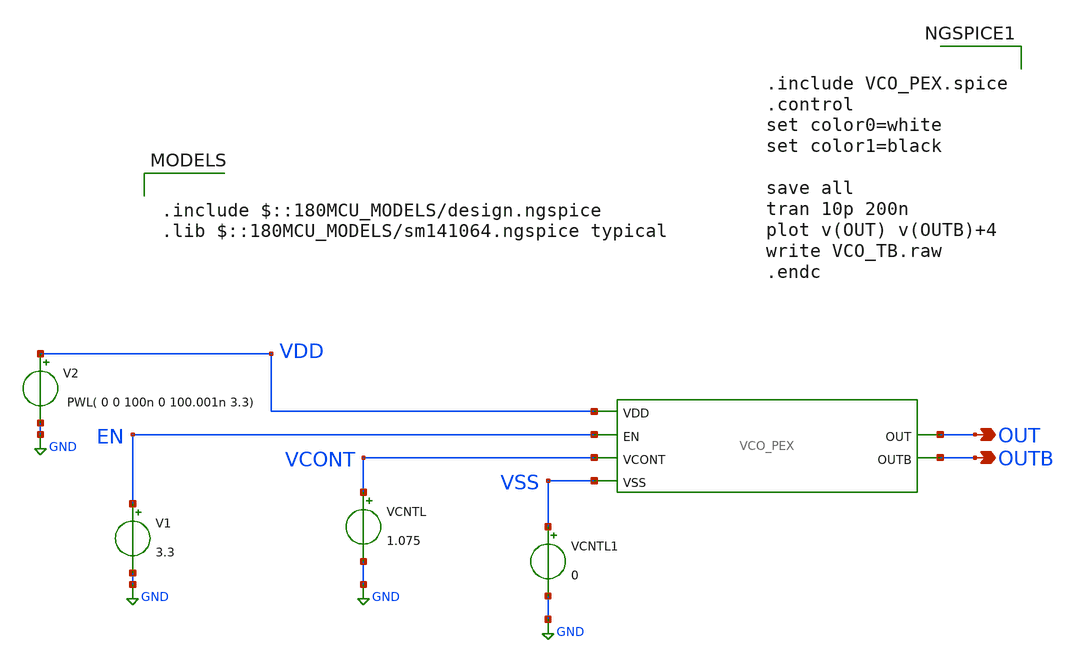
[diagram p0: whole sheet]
** sch_path: Clock_Generator_PAKISTAN_02/xschem/VCO_TB.sch
**.subckt VCO_TB OUT OUTB
*.opin OUT
*.opin OUTB
VCNTL VCONT GND 1.075
V2 VDD GND PWL( 0 0 100n 0 100.001n 3.3)
VCNTL1 VSS GND 0
V1 EN GND 3.3
x1 VDD EN OUT OUTB VCONT VSS VCO_PEX
**** begin user architecture code


.include VCO_PEX.spice
.control
set color0=white
set color1=black

save all
tran 10p 200n
plot v(OUT) v(OUTB)+4
write VCO_TB.raw
.endc



.include $::180MCU_MODELS/design.ngspice
.lib $::180MCU_MODELS/sm141064.ngspice typical

**** end user architecture code
**.ends
.GLOBAL GND
.end
